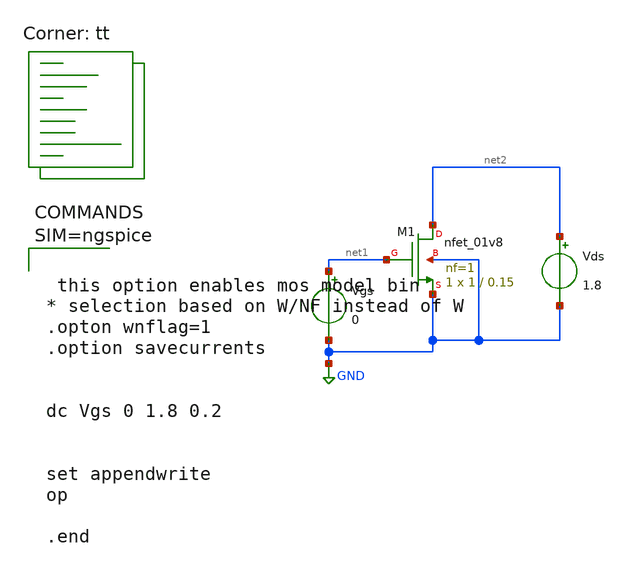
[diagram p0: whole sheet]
** sch_path: xschem/Polarizzazione0.sch
**.subckt Polarizzazione0
Vgs net1 GND 0
Vds net2 GND 1.8
XM1 net2 net1 GND GND sky130_fd_pr__nfet_01v8 L=0.15 W=1 nf=1 ad='int((nf+1)/2) * W/nf * 0.29' as='int((nf+2)/2) * W/nf * 0.29'
+ pd='2*int((nf+1)/2) * (W/nf + 0.29)' ps='2*int((nf+2)/2) * (W/nf + 0.29)' nrd='0.29 / W' nrs='0.29 / W'
+ sa=0 sb=0 sd=0 mult=1 m=1
**** begin user architecture code
.lib $::SKYWATER_MODELS/sky130.lib.spice tt



 this option enables mos model bin
* selection based on W/NF instead of W
.opton wnflag=1
.option savecurrents


dc Vgs 0 1.8 0.2


set appendwrite
op

.end




**** end user architecture code
**.ends
.GLOBAL GND
.end
